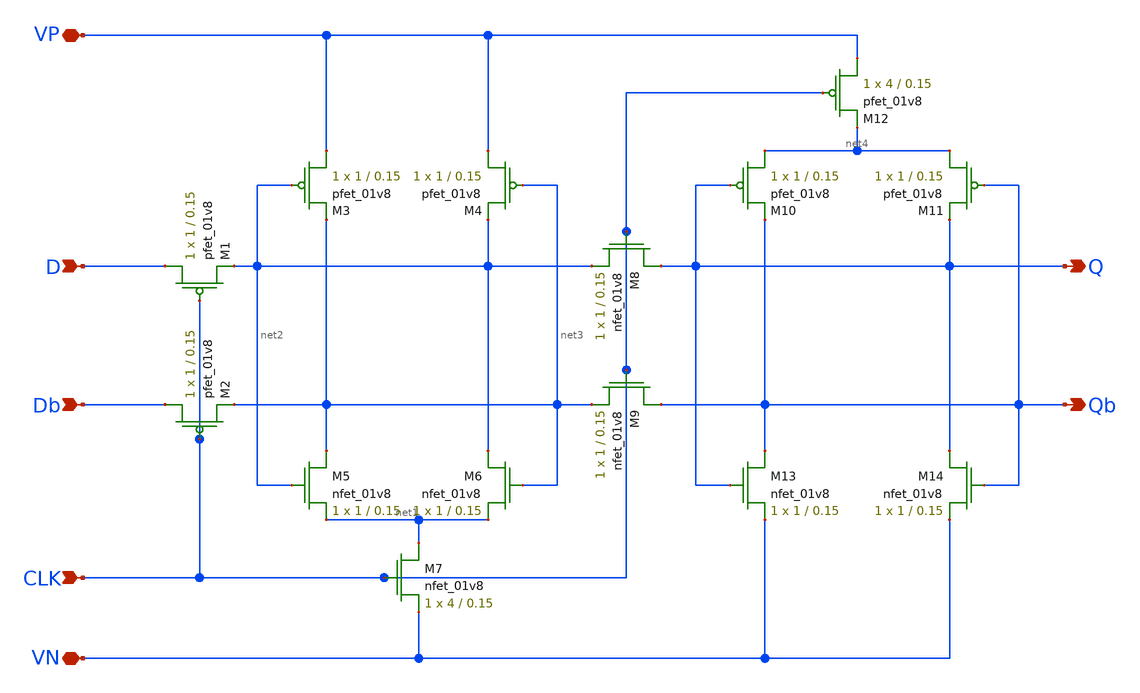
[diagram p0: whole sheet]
** sch_path: mp2/d_flipflop/d_flipflop.sch
**.subckt d_flipflop D CLK Q Qb Db VP VN
*.ipin D
*.ipin CLK
*.opin Q
*.opin Qb
*.ipin Db
*.iopin VP
*.iopin VN
XM1 D CLK net2 VP sky130_fd_pr__pfet_01v8 L=0.15 W=1 nf=1 ad='int((nf+1)/2) * W/nf * 0.29' as='int((nf+2)/2) * W/nf * 0.29'
+ pd='2*int((nf+1)/2) * (W/nf + 0.29)' ps='2*int((nf+2)/2) * (W/nf + 0.29)' nrd='0.29 / W' nrs='0.29 / W'
+ sa=0 sb=0 sd=0 mult=1 m=1
XM2 Db CLK net3 VP sky130_fd_pr__pfet_01v8 L=0.15 W=1 nf=1 ad='int((nf+1)/2) * W/nf * 0.29' as='int((nf+2)/2) * W/nf * 0.29'
+ pd='2*int((nf+1)/2) * (W/nf + 0.29)' ps='2*int((nf+2)/2) * (W/nf + 0.29)' nrd='0.29 / W' nrs='0.29 / W'
+ sa=0 sb=0 sd=0 mult=1 m=1
XM3 VP net2 net3 VP sky130_fd_pr__pfet_01v8 L=0.15 W=1 nf=1 ad='int((nf+1)/2) * W/nf * 0.29' as='int((nf+2)/2) * W/nf * 0.29'
+ pd='2*int((nf+1)/2) * (W/nf + 0.29)' ps='2*int((nf+2)/2) * (W/nf + 0.29)' nrd='0.29 / W' nrs='0.29 / W'
+ sa=0 sb=0 sd=0 mult=1 m=1
XM5 net3 net2 net1 VN sky130_fd_pr__nfet_01v8 L=0.15 W=1 nf=1 ad='int((nf+1)/2) * W/nf * 0.29' as='int((nf+2)/2) * W/nf * 0.29'
+ pd='2*int((nf+1)/2) * (W/nf + 0.29)' ps='2*int((nf+2)/2) * (W/nf + 0.29)' nrd='0.29 / W' nrs='0.29 / W'
+ sa=0 sb=0 sd=0 mult=1 m=1
XM7 net1 CLK VN VN sky130_fd_pr__nfet_01v8 L=0.15 W=4 nf=1 ad='int((nf+1)/2) * W/nf * 0.29' as='int((nf+2)/2) * W/nf * 0.29'
+ pd='2*int((nf+1)/2) * (W/nf + 0.29)' ps='2*int((nf+2)/2) * (W/nf + 0.29)' nrd='0.29 / W' nrs='0.29 / W'
+ sa=0 sb=0 sd=0 mult=1 m=1
XM8 Q CLK net2 VN sky130_fd_pr__nfet_01v8 L=0.15 W=1 nf=1 ad='int((nf+1)/2) * W/nf * 0.29' as='int((nf+2)/2) * W/nf * 0.29'
+ pd='2*int((nf+1)/2) * (W/nf + 0.29)' ps='2*int((nf+2)/2) * (W/nf + 0.29)' nrd='0.29 / W' nrs='0.29 / W'
+ sa=0 sb=0 sd=0 mult=1 m=1
XM9 Qb CLK net3 VN sky130_fd_pr__nfet_01v8 L=0.15 W=1 nf=1 ad='int((nf+1)/2) * W/nf * 0.29' as='int((nf+2)/2) * W/nf * 0.29'
+ pd='2*int((nf+1)/2) * (W/nf + 0.29)' ps='2*int((nf+2)/2) * (W/nf + 0.29)' nrd='0.29 / W' nrs='0.29 / W'
+ sa=0 sb=0 sd=0 mult=1 m=1
XM10 net4 Q Qb VP sky130_fd_pr__pfet_01v8 L=0.15 W=1 nf=1 ad='int((nf+1)/2) * W/nf * 0.29' as='int((nf+2)/2) * W/nf * 0.29'
+ pd='2*int((nf+1)/2) * (W/nf + 0.29)' ps='2*int((nf+2)/2) * (W/nf + 0.29)' nrd='0.29 / W' nrs='0.29 / W'
+ sa=0 sb=0 sd=0 mult=1 m=1
XM11 net4 Qb Q VP sky130_fd_pr__pfet_01v8 L=0.15 W=1 nf=1 ad='int((nf+1)/2) * W/nf * 0.29' as='int((nf+2)/2) * W/nf * 0.29'
+ pd='2*int((nf+1)/2) * (W/nf + 0.29)' ps='2*int((nf+2)/2) * (W/nf + 0.29)' nrd='0.29 / W' nrs='0.29 / W'
+ sa=0 sb=0 sd=0 mult=1 m=1
XM12 VP CLK net4 VP sky130_fd_pr__pfet_01v8 L=0.15 W=4 nf=1 ad='int((nf+1)/2) * W/nf * 0.29' as='int((nf+2)/2) * W/nf * 0.29'
+ pd='2*int((nf+1)/2) * (W/nf + 0.29)' ps='2*int((nf+2)/2) * (W/nf + 0.29)' nrd='0.29 / W' nrs='0.29 / W'
+ sa=0 sb=0 sd=0 mult=1 m=1
XM13 Qb Q VN VN sky130_fd_pr__nfet_01v8 L=0.15 W=1 nf=1 ad='int((nf+1)/2) * W/nf * 0.29' as='int((nf+2)/2) * W/nf * 0.29'
+ pd='2*int((nf+1)/2) * (W/nf + 0.29)' ps='2*int((nf+2)/2) * (W/nf + 0.29)' nrd='0.29 / W' nrs='0.29 / W'
+ sa=0 sb=0 sd=0 mult=1 m=1
XM14 Q Qb VN VN sky130_fd_pr__nfet_01v8 L=0.15 W=1 nf=1 ad='int((nf+1)/2) * W/nf * 0.29' as='int((nf+2)/2) * W/nf * 0.29'
+ pd='2*int((nf+1)/2) * (W/nf + 0.29)' ps='2*int((nf+2)/2) * (W/nf + 0.29)' nrd='0.29 / W' nrs='0.29 / W'
+ sa=0 sb=0 sd=0 mult=1 m=1
XM4 VP net3 net2 VP sky130_fd_pr__pfet_01v8 L=0.15 W=1 nf=1 ad='int((nf+1)/2) * W/nf * 0.29' as='int((nf+2)/2) * W/nf * 0.29'
+ pd='2*int((nf+1)/2) * (W/nf + 0.29)' ps='2*int((nf+2)/2) * (W/nf + 0.29)' nrd='0.29 / W' nrs='0.29 / W'
+ sa=0 sb=0 sd=0 mult=1 m=1
XM6 net2 net3 net1 VN sky130_fd_pr__nfet_01v8 L=0.15 W=1 nf=1 ad='int((nf+1)/2) * W/nf * 0.29' as='int((nf+2)/2) * W/nf * 0.29'
+ pd='2*int((nf+1)/2) * (W/nf + 0.29)' ps='2*int((nf+2)/2) * (W/nf + 0.29)' nrd='0.29 / W' nrs='0.29 / W'
+ sa=0 sb=0 sd=0 mult=1 m=1
**.ends
.end
